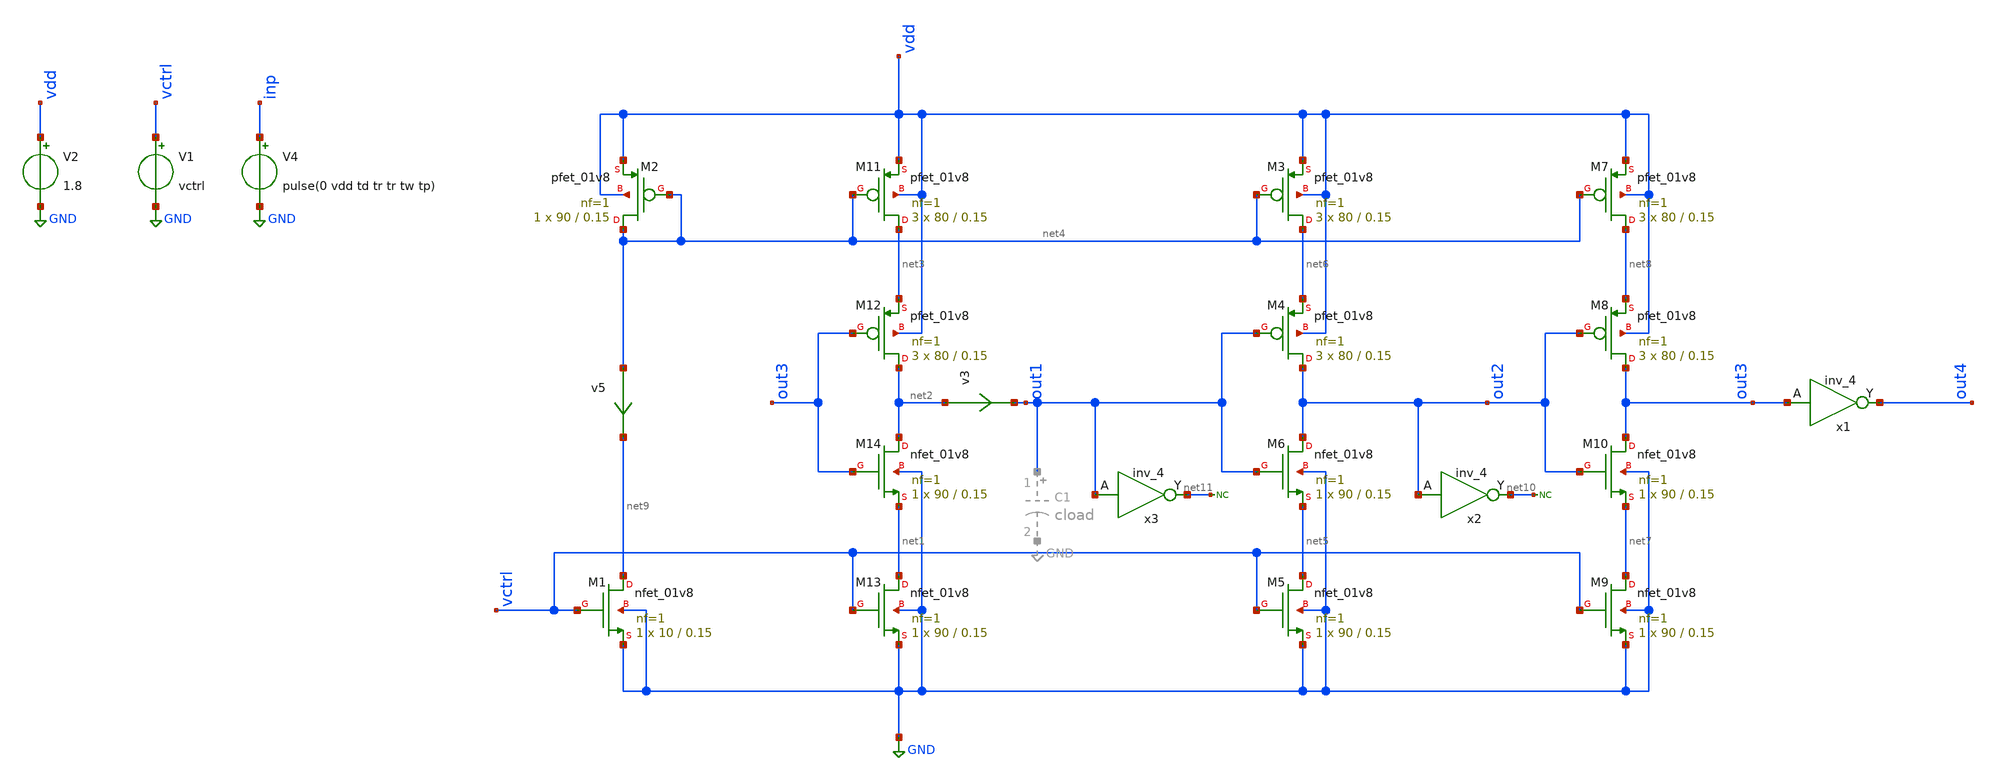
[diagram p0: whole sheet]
** sch_path: xschem/inv_delay (1).sch
**.subckt inv_delay (1)
XM1 net9 vctrl GND GND sky130_fd_pr__nfet_01v8 L=0.15 W=10 nf=1 ad='int((nf+1)/2) * W/nf * 0.29' as='int((nf+2)/2) * W/nf * 0.29'
+ pd='2*int((nf+1)/2) * (W/nf + 0.29)' ps='2*int((nf+2)/2) * (W/nf + 0.29)' nrd='0.29 / W' nrs='0.29 / W'
+ sa=0 sb=0 sd=0 mult=1 m=1
XM2 net4 net4 vdd vdd sky130_fd_pr__pfet_01v8 L=0.15 W=90 nf=1 ad='int((nf+1)/2) * W/nf * 0.29' as='int((nf+2)/2) * W/nf * 0.29'
+ pd='2*int((nf+1)/2) * (W/nf + 0.29)' ps='2*int((nf+2)/2) * (W/nf + 0.29)' nrd='0.29 / W' nrs='0.29 / W'
+ sa=0 sb=0 sd=0 mult=1 m=1
XM11 net3 net4 vdd vdd sky130_fd_pr__pfet_01v8 L=0.15 W=80 nf=1 ad='int((nf+1)/2) * W/nf * 0.29' as='int((nf+2)/2) * W/nf * 0.29'
+ pd='2*int((nf+1)/2) * (W/nf + 0.29)' ps='2*int((nf+2)/2) * (W/nf + 0.29)' nrd='0.29 / W' nrs='0.29 / W'
+ sa=0 sb=0 sd=0 mult=3 m=3
XM12 net2 out3 net3 vdd sky130_fd_pr__pfet_01v8 L=0.15 W=80 nf=1 ad='int((nf+1)/2) * W/nf * 0.29' as='int((nf+2)/2) * W/nf * 0.29'
+ pd='2*int((nf+1)/2) * (W/nf + 0.29)' ps='2*int((nf+2)/2) * (W/nf + 0.29)' nrd='0.29 / W' nrs='0.29 / W'
+ sa=0 sb=0 sd=0 mult=3 m=3
XM13 net1 vctrl GND GND sky130_fd_pr__nfet_01v8 L=0.15 W=90 nf=1 ad='int((nf+1)/2) * W/nf * 0.29' as='int((nf+2)/2) * W/nf * 0.29'
+ pd='2*int((nf+1)/2) * (W/nf + 0.29)' ps='2*int((nf+2)/2) * (W/nf + 0.29)' nrd='0.29 / W' nrs='0.29 / W'
+ sa=0 sb=0 sd=0 mult=1 m=1
XM14 net2 out3 net1 GND sky130_fd_pr__nfet_01v8 L=0.15 W=90 nf=1 ad='int((nf+1)/2) * W/nf * 0.29' as='int((nf+2)/2) * W/nf * 0.29'
+ pd='2*int((nf+1)/2) * (W/nf + 0.29)' ps='2*int((nf+2)/2) * (W/nf + 0.29)' nrd='0.29 / W' nrs='0.29 / W'
+ sa=0 sb=0 sd=0 mult=1 m=1
V1 vctrl GND vctrl
V2 vdd GND 1.8
V4 inp GND pulse(0 vdd td tr tr tw tp)
XM3 net6 net4 vdd vdd sky130_fd_pr__pfet_01v8 L=0.15 W=80 nf=1 ad='int((nf+1)/2) * W/nf * 0.29' as='int((nf+2)/2) * W/nf * 0.29'
+ pd='2*int((nf+1)/2) * (W/nf + 0.29)' ps='2*int((nf+2)/2) * (W/nf + 0.29)' nrd='0.29 / W' nrs='0.29 / W'
+ sa=0 sb=0 sd=0 mult=3 m=3
XM4 out2 out1 net6 vdd sky130_fd_pr__pfet_01v8 L=0.15 W=80 nf=1 ad='int((nf+1)/2) * W/nf * 0.29' as='int((nf+2)/2) * W/nf * 0.29'
+ pd='2*int((nf+1)/2) * (W/nf + 0.29)' ps='2*int((nf+2)/2) * (W/nf + 0.29)' nrd='0.29 / W' nrs='0.29 / W'
+ sa=0 sb=0 sd=0 mult=3 m=3
XM5 net5 vctrl GND GND sky130_fd_pr__nfet_01v8 L=0.15 W=90 nf=1 ad='int((nf+1)/2) * W/nf * 0.29' as='int((nf+2)/2) * W/nf * 0.29'
+ pd='2*int((nf+1)/2) * (W/nf + 0.29)' ps='2*int((nf+2)/2) * (W/nf + 0.29)' nrd='0.29 / W' nrs='0.29 / W'
+ sa=0 sb=0 sd=0 mult=1 m=1
XM6 out2 out1 net5 GND sky130_fd_pr__nfet_01v8 L=0.15 W=90 nf=1 ad='int((nf+1)/2) * W/nf * 0.29' as='int((nf+2)/2) * W/nf * 0.29'
+ pd='2*int((nf+1)/2) * (W/nf + 0.29)' ps='2*int((nf+2)/2) * (W/nf + 0.29)' nrd='0.29 / W' nrs='0.29 / W'
+ sa=0 sb=0 sd=0 mult=1 m=1
XM7 net8 net4 vdd vdd sky130_fd_pr__pfet_01v8 L=0.15 W=80 nf=1 ad='int((nf+1)/2) * W/nf * 0.29' as='int((nf+2)/2) * W/nf * 0.29'
+ pd='2*int((nf+1)/2) * (W/nf + 0.29)' ps='2*int((nf+2)/2) * (W/nf + 0.29)' nrd='0.29 / W' nrs='0.29 / W'
+ sa=0 sb=0 sd=0 mult=3 m=3
XM8 out3 out2 net8 vdd sky130_fd_pr__pfet_01v8 L=0.15 W=80 nf=1 ad='int((nf+1)/2) * W/nf * 0.29' as='int((nf+2)/2) * W/nf * 0.29'
+ pd='2*int((nf+1)/2) * (W/nf + 0.29)' ps='2*int((nf+2)/2) * (W/nf + 0.29)' nrd='0.29 / W' nrs='0.29 / W'
+ sa=0 sb=0 sd=0 mult=3 m=3
XM9 net7 vctrl GND GND sky130_fd_pr__nfet_01v8 L=0.15 W=90 nf=1 ad='int((nf+1)/2) * W/nf * 0.29' as='int((nf+2)/2) * W/nf * 0.29'
+ pd='2*int((nf+1)/2) * (W/nf + 0.29)' ps='2*int((nf+2)/2) * (W/nf + 0.29)' nrd='0.29 / W' nrs='0.29 / W'
+ sa=0 sb=0 sd=0 mult=1 m=1
XM10 out3 out2 net7 GND sky130_fd_pr__nfet_01v8 L=0.15 W=90 nf=1 ad='int((nf+1)/2) * W/nf * 0.29' as='int((nf+2)/2) * W/nf * 0.29'
+ pd='2*int((nf+1)/2) * (W/nf + 0.29)' ps='2*int((nf+2)/2) * (W/nf + 0.29)' nrd='0.29 / W' nrs='0.29 / W'
+ sa=0 sb=0 sd=0 mult=1 m=1
x1 out3 GND GND VDD VDD out4 sky130_fd_sc_hd__inv_4
v3 net2 out1 0
.save i(v3)
v5 net4 net9 0
.save i(v5)
x2 out2 GND GND VDD VDD net10 sky130_fd_sc_hd__inv_4
* noconn #net10
x3 out1 GND GND VDD VDD net11 sky130_fd_sc_hd__inv_4
* noconn #net11
**** begin user architecture code


.options acct list
.temp 25
.save all
.save @m.xm1.msky130_fd_pr__nfet_01v8[cgd]
.save @m.xm1.msky130_fd_pr__nfet_01v8[gm]

.param vctrl=0.82 vdd=1.8 cload=250f  td=20n tr=0.1n tw=10n  tp=20n

.control
op
write inv_delay.raw
set appendwrite

tran 0.001n 100n uic
meas tran tdelay01 TRIG v(out4) VAL=0.9 RISE=15 TARG v(out4) VAL=0.9 RISE=16
let fosc1= 1/tdelay01
print fosc1
save fosc1
remzerovec
write inv_delay.raw


alterparam vctrl=0.75
reset
set appendwrite
tran 0.001n 100n uic
meas tran tdelay01 TRIG v(out4) VAL=0.9 RISE=15 TARG v(out4) VAL=0.9 RISE=16
let fosc1= 1/tdelay01
print fosc1
save fosc1
remzerovec
write inv_delay.raw

.endc



** opencircuitdesign pdks install
.lib $::SKYWATER_MODELS/sky130.lib.spice tt
.include $::SKYWATER_STDCELLS/sky130_fd_sc_hd.spice


**** end user architecture code
**.ends
.GLOBAL GND
.end
